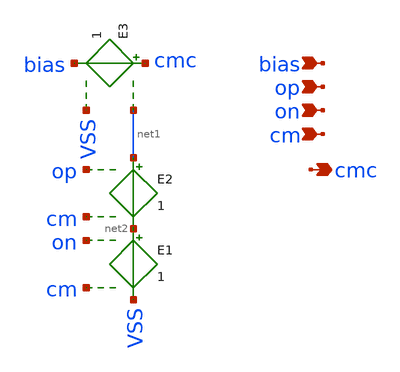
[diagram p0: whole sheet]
** sch_path: design/schematic/ideal_cmfb.sch
**.subckt ideal_cmfb bias op on cm cmc
*.ipin bias
*.ipin op
*.ipin on
*.ipin cm
*.opin cmc
E1 net2 VSS on cm 1
E2 net1 net2 op cm 1
E3 cmc bias net1 VSS 1
**.ends
.end
